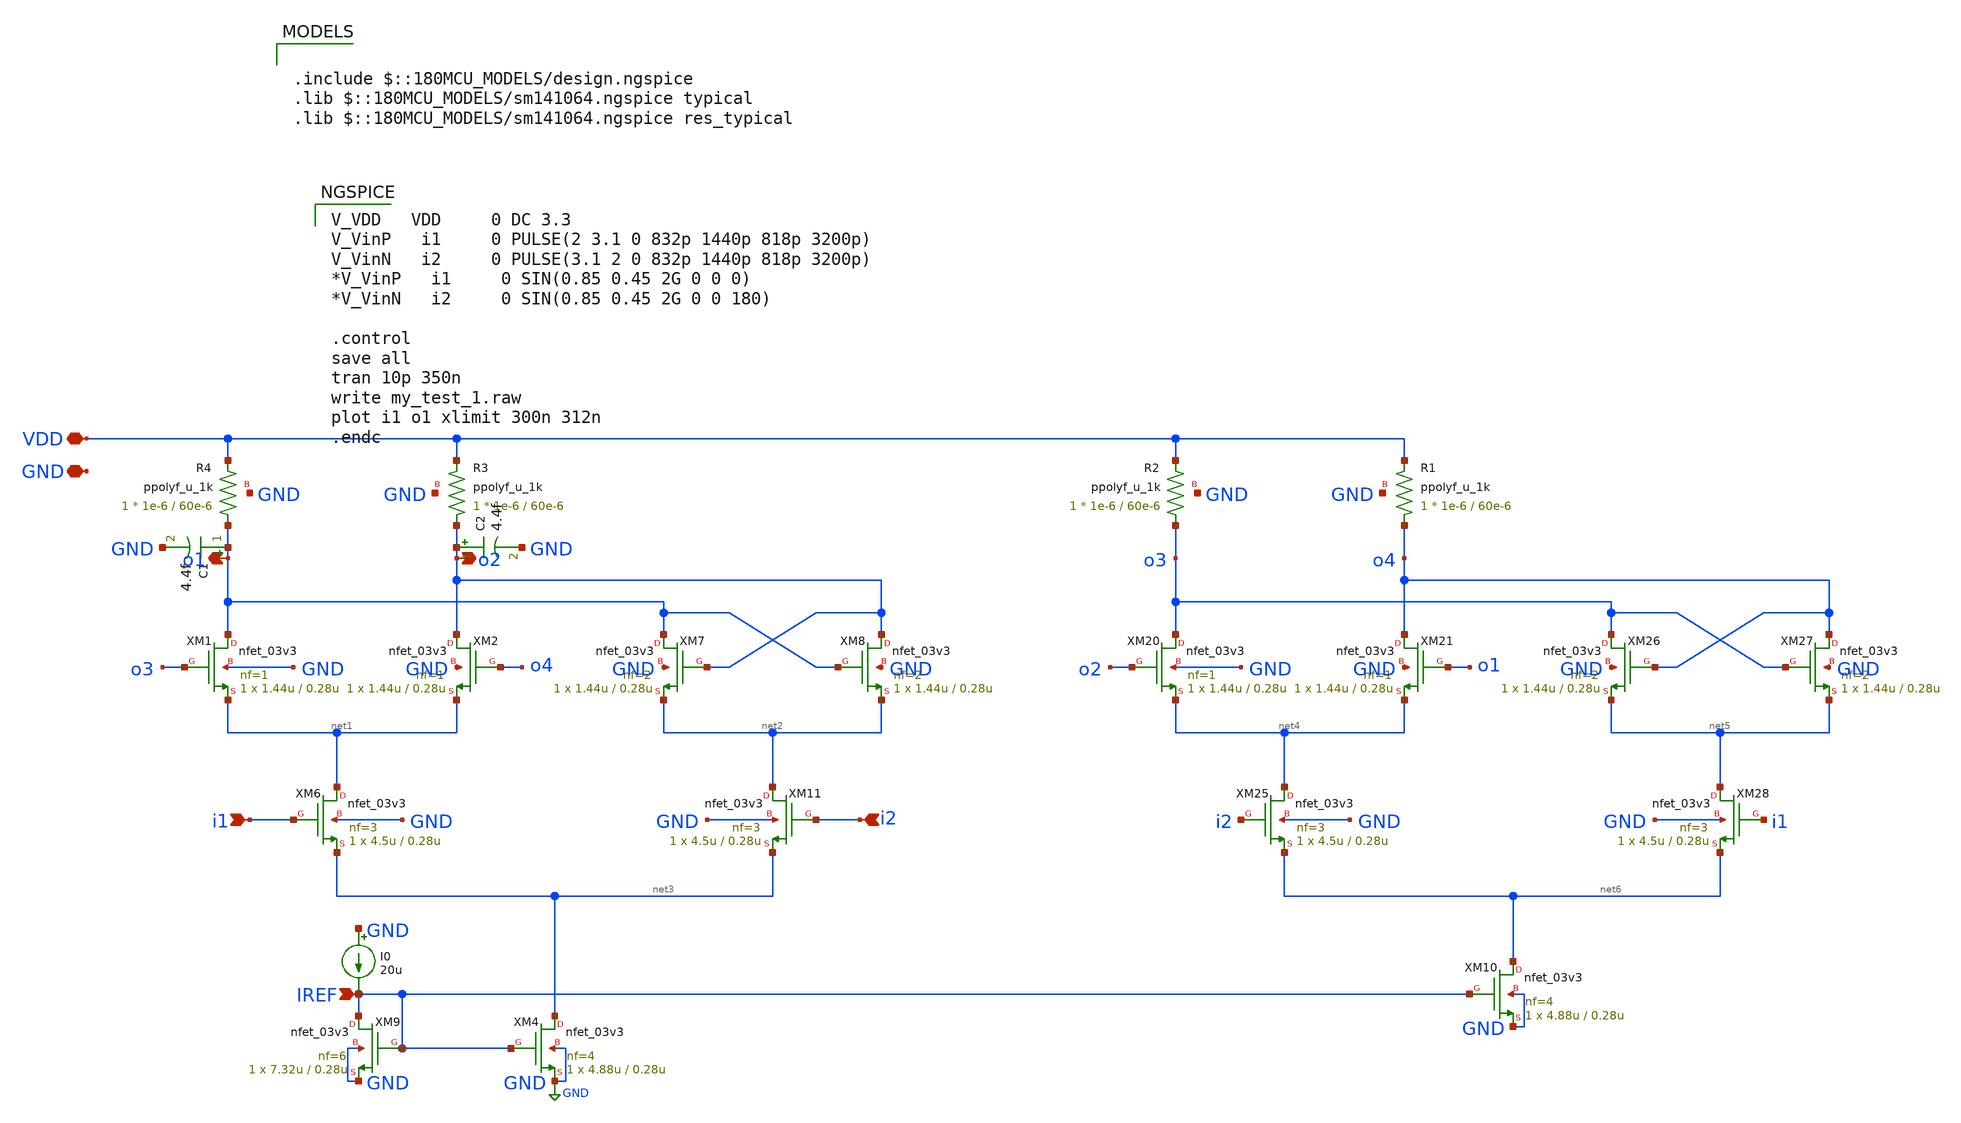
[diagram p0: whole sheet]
** sch_path: rha-vga-pll-blocks/blocks/pll/cml_div_5.sch
**.subckt cml_div_5 i2 i1 o2 o1 VDD GND IREF
*.ipin i2
*.ipin i1
*.opin o2
*.opin o1
*.iopin VDD
*.iopin GND
*.ipin IREF
XM1 o1 o3 net1 GND nfet_03v3 L=0.28u W=1.44u nf=1 ad='int((nf+1)/2) * W/nf * 0.18u' as='int((nf+2)/2) * W/nf * 0.18u'
+ pd='2*int((nf+1)/2) * (W/nf + 0.18u)' ps='2*int((nf+2)/2) * (W/nf + 0.18u)' nrd='0.18u / W' nrs='0.18u / W'
+ sa=0 sb=0 sd=0 m=1
XM2 o2 o4 net1 GND nfet_03v3 L=0.28u W=1.44u nf=1 ad='int((nf+1)/2) * W/nf * 0.18u' as='int((nf+2)/2) * W/nf * 0.18u'
+ pd='2*int((nf+1)/2) * (W/nf + 0.18u)' ps='2*int((nf+2)/2) * (W/nf + 0.18u)' nrd='0.18u / W' nrs='0.18u / W'
+ sa=0 sb=0 sd=0 m=1
XM4 net3 IREF GND GND nfet_03v3 L=0.28u W=4.88u nf=4 ad='int((nf+1)/2) * W/nf * 0.18u' as='int((nf+2)/2) * W/nf * 0.18u'
+ pd='2*int((nf+1)/2) * (W/nf + 0.18u)' ps='2*int((nf+2)/2) * (W/nf + 0.18u)' nrd='0.18u / W' nrs='0.18u / W'
+ sa=0 sb=0 sd=0 m=1
XM6 net1 i1 net3 GND nfet_03v3 L=0.28u W=4.5u nf=3 ad='int((nf+1)/2) * W/nf * 0.18u' as='int((nf+2)/2) * W/nf * 0.18u'
+ pd='2*int((nf+1)/2) * (W/nf + 0.18u)' ps='2*int((nf+2)/2) * (W/nf + 0.18u)' nrd='0.18u / W' nrs='0.18u / W'
+ sa=0 sb=0 sd=0 m=1
XM7 o1 o2 net2 GND nfet_03v3 L=0.28u W=1.44u nf=2 ad='int((nf+1)/2) * W/nf * 0.18u' as='int((nf+2)/2) * W/nf * 0.18u'
+ pd='2*int((nf+1)/2) * (W/nf + 0.18u)' ps='2*int((nf+2)/2) * (W/nf + 0.18u)' nrd='0.18u / W' nrs='0.18u / W'
+ sa=0 sb=0 sd=0 m=1
XM8 o2 o1 net2 GND nfet_03v3 L=0.28u W=1.44u nf=2 ad='int((nf+1)/2) * W/nf * 0.18u' as='int((nf+2)/2) * W/nf * 0.18u'
+ pd='2*int((nf+1)/2) * (W/nf + 0.18u)' ps='2*int((nf+2)/2) * (W/nf + 0.18u)' nrd='0.18u / W' nrs='0.18u / W'
+ sa=0 sb=0 sd=0 m=1
XM11 net2 i2 net3 GND nfet_03v3 L=0.28u W=4.5u nf=3 ad='int((nf+1)/2) * W/nf * 0.18u' as='int((nf+2)/2) * W/nf * 0.18u'
+ pd='2*int((nf+1)/2) * (W/nf + 0.18u)' ps='2*int((nf+2)/2) * (W/nf + 0.18u)' nrd='0.18u / W' nrs='0.18u / W'
+ sa=0 sb=0 sd=0 m=1
XM9 IREF IREF GND GND nfet_03v3 L=0.28u W=7.32u nf=6 ad='int((nf+1)/2) * W/nf * 0.18u' as='int((nf+2)/2) * W/nf * 0.18u'
+ pd='2*int((nf+1)/2) * (W/nf + 0.18u)' ps='2*int((nf+2)/2) * (W/nf + 0.18u)' nrd='0.18u / W' nrs='0.18u / W'
+ sa=0 sb=0 sd=0 m=1
XM20 o3 o2 net4 GND nfet_03v3 L=0.28u W=1.44u nf=1 ad='int((nf+1)/2) * W/nf * 0.18u' as='int((nf+2)/2) * W/nf * 0.18u'
+ pd='2*int((nf+1)/2) * (W/nf + 0.18u)' ps='2*int((nf+2)/2) * (W/nf + 0.18u)' nrd='0.18u / W' nrs='0.18u / W'
+ sa=0 sb=0 sd=0 m=1
XM21 o4 o1 net4 GND nfet_03v3 L=0.28u W=1.44u nf=1 ad='int((nf+1)/2) * W/nf * 0.18u' as='int((nf+2)/2) * W/nf * 0.18u'
+ pd='2*int((nf+1)/2) * (W/nf + 0.18u)' ps='2*int((nf+2)/2) * (W/nf + 0.18u)' nrd='0.18u / W' nrs='0.18u / W'
+ sa=0 sb=0 sd=0 m=1
XM25 net4 i2 net6 GND nfet_03v3 L=0.28u W=4.5u nf=3 ad='int((nf+1)/2) * W/nf * 0.18u' as='int((nf+2)/2) * W/nf * 0.18u'
+ pd='2*int((nf+1)/2) * (W/nf + 0.18u)' ps='2*int((nf+2)/2) * (W/nf + 0.18u)' nrd='0.18u / W' nrs='0.18u / W'
+ sa=0 sb=0 sd=0 m=1
XM26 o3 o4 net5 GND nfet_03v3 L=0.28u W=1.44u nf=2 ad='int((nf+1)/2) * W/nf * 0.18u' as='int((nf+2)/2) * W/nf * 0.18u'
+ pd='2*int((nf+1)/2) * (W/nf + 0.18u)' ps='2*int((nf+2)/2) * (W/nf + 0.18u)' nrd='0.18u / W' nrs='0.18u / W'
+ sa=0 sb=0 sd=0 m=1
XM27 o4 o3 net5 GND nfet_03v3 L=0.28u W=1.44u nf=2 ad='int((nf+1)/2) * W/nf * 0.18u' as='int((nf+2)/2) * W/nf * 0.18u'
+ pd='2*int((nf+1)/2) * (W/nf + 0.18u)' ps='2*int((nf+2)/2) * (W/nf + 0.18u)' nrd='0.18u / W' nrs='0.18u / W'
+ sa=0 sb=0 sd=0 m=1
XM28 net5 i1 net6 GND nfet_03v3 L=0.28u W=4.5u nf=3 ad='int((nf+1)/2) * W/nf * 0.18u' as='int((nf+2)/2) * W/nf * 0.18u'
+ pd='2*int((nf+1)/2) * (W/nf + 0.18u)' ps='2*int((nf+2)/2) * (W/nf + 0.18u)' nrd='0.18u / W' nrs='0.18u / W'
+ sa=0 sb=0 sd=0 m=1
XM10 net6 IREF GND GND nfet_03v3 L=0.28u W=4.88u nf=4 ad='int((nf+1)/2) * W/nf * 0.18u' as='int((nf+2)/2) * W/nf * 0.18u'
+ pd='2*int((nf+1)/2) * (W/nf + 0.18u)' ps='2*int((nf+2)/2) * (W/nf + 0.18u)' nrd='0.18u / W' nrs='0.18u / W'
+ sa=0 sb=0 sd=0 m=1
I0 GND IREF 20u
XR1 o4 VDD GND ppolyf_u_1k r_width=1e-6 r_length=60e-6 m=1
XR2 o3 VDD GND ppolyf_u_1k r_width=1e-6 r_length=60e-6 m=1
XR3 o2 VDD GND ppolyf_u_1k r_width=1e-6 r_length=60e-6 m=1
XR4 o1 VDD GND ppolyf_u_1k r_width=1e-6 r_length=60e-6 m=1
C1 o1 GND 4.4f m=1
C2 o2 GND 4.4f m=1
**** begin user architecture code

.include $::180MCU_MODELS/design.ngspice
.lib $::180MCU_MODELS/sm141064.ngspice typical
.lib $::180MCU_MODELS/sm141064.ngspice res_typical


V_VDD   VDD     0 DC 3.3
V_VinP   i1     0 PULSE(2 3.1 0 832p 1440p 818p 3200p)
V_VinN   i2     0 PULSE(3.1 2 0 832p 1440p 818p 3200p)
*V_VinP   i1     0 SIN(0.85 0.45 2G 0 0 0)
*V_VinN   i2     0 SIN(0.85 0.45 2G 0 0 180)

.control
save all
tran 10p 350n
write my_test_1.raw
plot i1 o1 xlimit 300n 312n
.endc


**** end user architecture code
**.ends
.GLOBAL GND
.end
